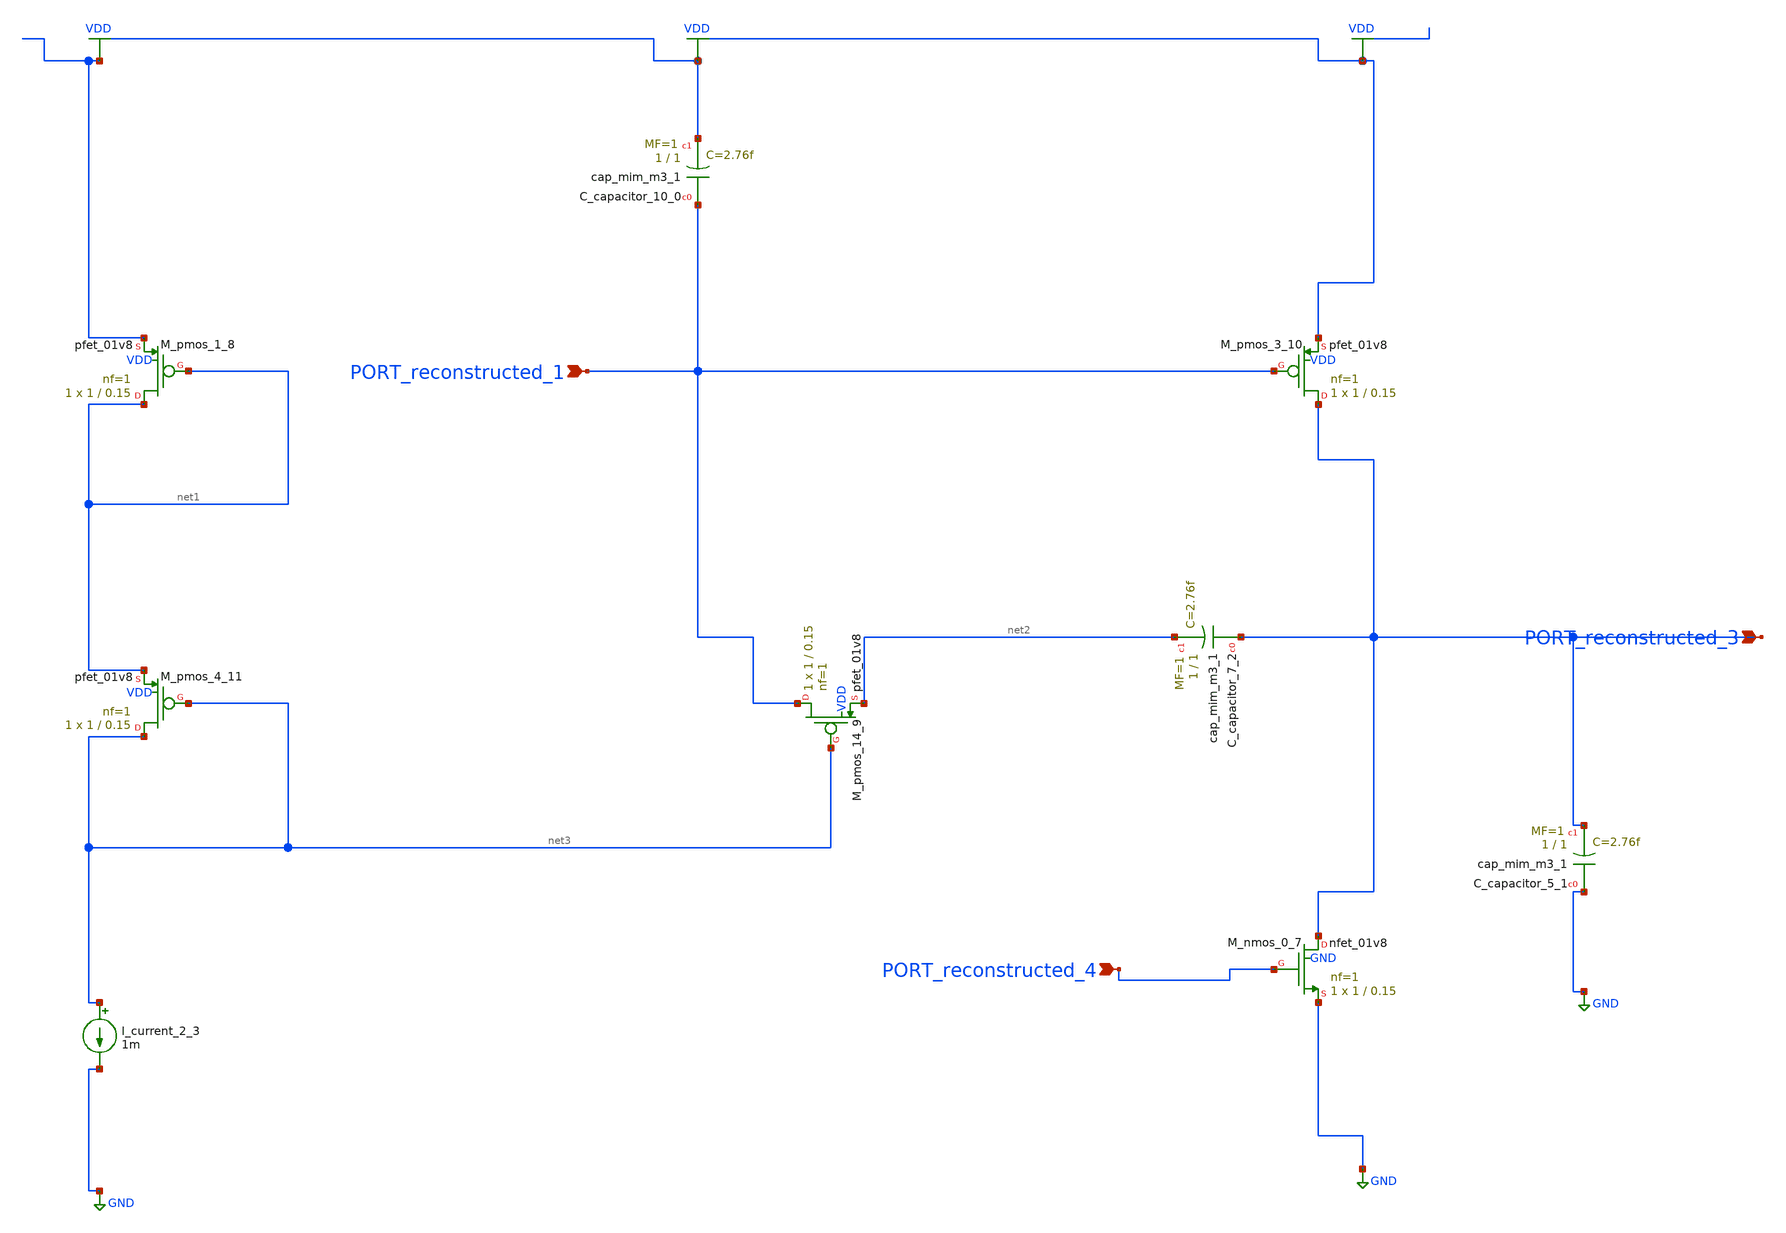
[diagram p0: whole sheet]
** sch_path: schematics/AMSNet/726.sch
**.subckt 726 PORT_reconstructed_4 PORT_reconstructed_1 PORT_reconstructed_3
*.ipin PORT_reconstructed_4
*.ipin PORT_reconstructed_1
*.ipin PORT_reconstructed_3
XC_capacitor_10_0 PORT_reconstructed_1 VDD sky130_fd_pr__cap_mim_m3_1 W=1 L=1 MF=1 m=1
XC_capacitor_5_1 GND PORT_reconstructed_3 sky130_fd_pr__cap_mim_m3_1 W=1 L=1 MF=1 m=1
XC_capacitor_7_2 PORT_reconstructed_3 net2 sky130_fd_pr__cap_mim_m3_1 W=1 L=1 MF=1 m=1
I_current_2_3 net3 GND 1m
XM_nmos_0_7 PORT_reconstructed_3 PORT_reconstructed_4 GND GND sky130_fd_pr__nfet_01v8 L=0.15 W=1 nf=1
+ ad='int((1 + 1)/2) * 1 / 1 * 0.29' as='int((1 + 2)/2) * 1 / 1 * 0.29' pd='2*int((1 + 1)/2) * (1 / 1 + 0.29)'
+ ps='2*int((1 + 2)/2) * (1 / 1 + 0.29)' nrd='0.29 / 1 ' nrs='0.29 / 1 ' sa=0 sb=0 sd=0 mult=1 m=1
XM_pmos_1_8 net1 net1 VDD VDD sky130_fd_pr__pfet_01v8 L=0.15 W=1 nf=1 ad='int((1 + 1)/2) * 1 / 1 * 0.29'
+ as='int((1 + 2)/2) * 1 / 1 * 0.29' pd='2*int((1 + 1)/2) * (1 / 1 + 0.29)' ps='2*int((1 + 2)/2) * (1 / 1 + 0.29)'
+ nrd='0.29 / 1 ' nrs='0.29 / 1 ' sa=0 sb=0 sd=0 mult=1 m=1
XM_pmos_14_9 PORT_reconstructed_1 net3 net2 VDD sky130_fd_pr__pfet_01v8 L=0.15 W=1 nf=1 ad='int((1 + 1)/2) * 1 / 1 * 0.29'
+ as='int((1 + 2)/2) * 1 / 1 * 0.29' pd='2*int((1 + 1)/2) * (1 / 1 + 0.29)' ps='2*int((1 + 2)/2) * (1 / 1 + 0.29)'
+ nrd='0.29 / 1 ' nrs='0.29 / 1 ' sa=0 sb=0 sd=0 mult=1 m=1
XM_pmos_3_10 PORT_reconstructed_3 PORT_reconstructed_1 VDD VDD sky130_fd_pr__pfet_01v8 L=0.15 W=1 nf=1
+ ad='int((1 + 1)/2) * 1 / 1 * 0.29' as='int((1 + 2)/2) * 1 / 1 * 0.29' pd='2*int((1 + 1)/2) * (1 / 1 + 0.29)'
+ ps='2*int((1 + 2)/2) * (1 / 1 + 0.29)' nrd='0.29 / 1 ' nrs='0.29 / 1 ' sa=0 sb=0 sd=0 mult=1 m=1
XM_pmos_4_11 net3 net3 net1 VDD sky130_fd_pr__pfet_01v8 L=0.15 W=1 nf=1 ad='int((1 + 1)/2) * 1 / 1 * 0.29'
+ as='int((1 + 2)/2) * 1 / 1 * 0.29' pd='2*int((1 + 1)/2) * (1 / 1 + 0.29)' ps='2*int((1 + 2)/2) * (1 / 1 + 0.29)'
+ nrd='0.29 / 1 ' nrs='0.29 / 1 ' sa=0 sb=0 sd=0 mult=1 m=1
**.ends
.GLOBAL GND
.GLOBAL VDD
.end
